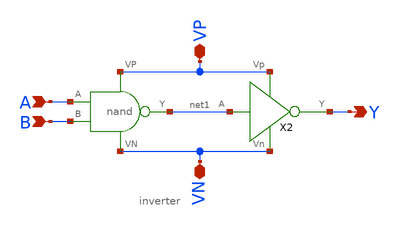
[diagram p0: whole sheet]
** sch_path: mini_proj_1/schematic/and.sch
**.subckt and A B VP VN Y
*.ipin A
*.ipin B
*.iopin VP
*.iopin VN
*.opin Y
X1 A B VP VN net1 nand
X2 net1 VN VP Y inverter
**.ends
.end
